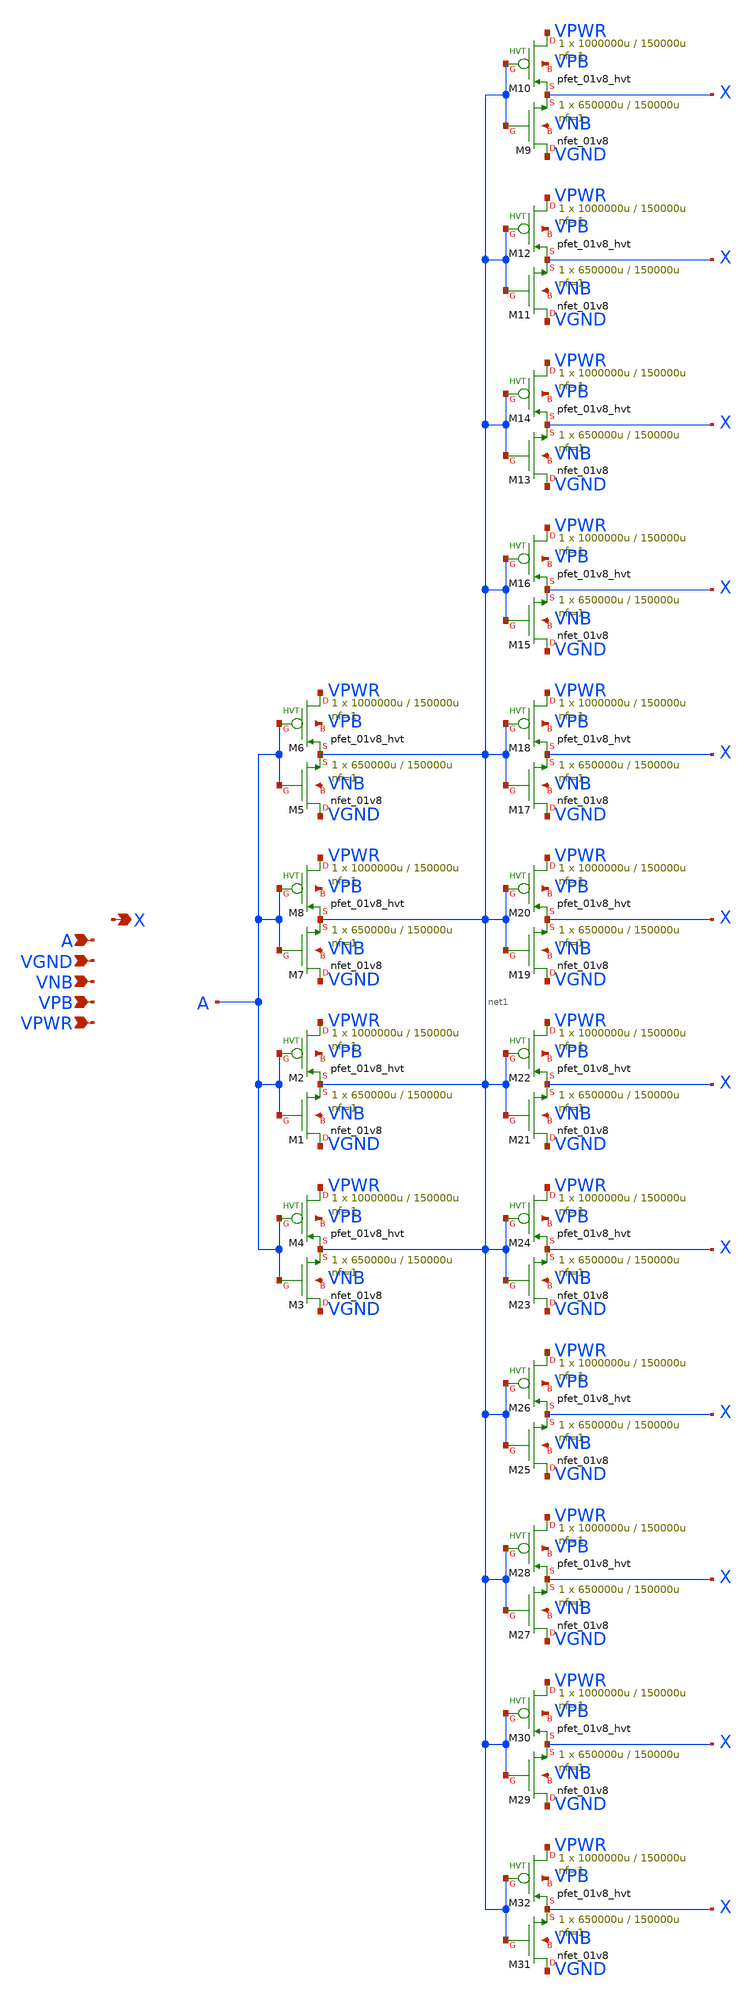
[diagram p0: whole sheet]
** sch_path: schematics/buf/sky130_fd_sc_hd__buf_12.sch
**.subckt sky130_fd_sc_hd__buf_12 A VGND VNB VPB VPWR X
*.ipin A
*.ipin VGND
*.ipin VNB
*.ipin VPB
*.ipin VPWR
*.opin X
XM1 VGND A net1 VNB sky130_fd_pr__nfet_01v8 L=150000u W=650000u nf=1 ad='int((1 + 1)/2) * 650000u / 1 * 0.29'
+ as='int((1 + 2)/2) * 650000u / 1 * 0.29' pd='2*int((1 + 1)/2) * (650000u / 1 + 0.29)' ps='2*int((1 + 2)/2) * (650000u / 1 + 0.29)'
+ nrd='0.29 / 650000u ' nrs='0.29 / 650000u ' sa=0 sb=0 sd=0 mult=1 m=1
XM2 VPWR A net1 VPB sky130_fd_pr__pfet_01v8_hvt L=150000u W=1000000u nf=1 ad='int((1 + 1)/2) * 1000000u / 1 * 0.29'
+ as='int((1 + 2)/2) * 1000000u / 1 * 0.29' pd='2*int((1 + 1)/2) * (1000000u / 1 + 0.29)' ps='2*int((1 + 2)/2) * (1000000u / 1 + 0.29)'
+ nrd='0.29 / 1000000u ' nrs='0.29 / 1000000u ' sa=0 sb=0 sd=0 mult=1 m=1
XM3 VGND A net1 VNB sky130_fd_pr__nfet_01v8 L=150000u W=650000u nf=1 ad='int((1 + 1)/2) * 650000u / 1 * 0.29'
+ as='int((1 + 2)/2) * 650000u / 1 * 0.29' pd='2*int((1 + 1)/2) * (650000u / 1 + 0.29)' ps='2*int((1 + 2)/2) * (650000u / 1 + 0.29)'
+ nrd='0.29 / 650000u ' nrs='0.29 / 650000u ' sa=0 sb=0 sd=0 mult=1 m=1
XM4 VPWR A net1 VPB sky130_fd_pr__pfet_01v8_hvt L=150000u W=1000000u nf=1 ad='int((1 + 1)/2) * 1000000u / 1 * 0.29'
+ as='int((1 + 2)/2) * 1000000u / 1 * 0.29' pd='2*int((1 + 1)/2) * (1000000u / 1 + 0.29)' ps='2*int((1 + 2)/2) * (1000000u / 1 + 0.29)'
+ nrd='0.29 / 1000000u ' nrs='0.29 / 1000000u ' sa=0 sb=0 sd=0 mult=1 m=1
XM5 VGND A net1 VNB sky130_fd_pr__nfet_01v8 L=150000u W=650000u nf=1 ad='int((1 + 1)/2) * 650000u / 1 * 0.29'
+ as='int((1 + 2)/2) * 650000u / 1 * 0.29' pd='2*int((1 + 1)/2) * (650000u / 1 + 0.29)' ps='2*int((1 + 2)/2) * (650000u / 1 + 0.29)'
+ nrd='0.29 / 650000u ' nrs='0.29 / 650000u ' sa=0 sb=0 sd=0 mult=1 m=1
XM6 VPWR A net1 VPB sky130_fd_pr__pfet_01v8_hvt L=150000u W=1000000u nf=1 ad='int((1 + 1)/2) * 1000000u / 1 * 0.29'
+ as='int((1 + 2)/2) * 1000000u / 1 * 0.29' pd='2*int((1 + 1)/2) * (1000000u / 1 + 0.29)' ps='2*int((1 + 2)/2) * (1000000u / 1 + 0.29)'
+ nrd='0.29 / 1000000u ' nrs='0.29 / 1000000u ' sa=0 sb=0 sd=0 mult=1 m=1
XM7 VGND A net1 VNB sky130_fd_pr__nfet_01v8 L=150000u W=650000u nf=1 ad='int((1 + 1)/2) * 650000u / 1 * 0.29'
+ as='int((1 + 2)/2) * 650000u / 1 * 0.29' pd='2*int((1 + 1)/2) * (650000u / 1 + 0.29)' ps='2*int((1 + 2)/2) * (650000u / 1 + 0.29)'
+ nrd='0.29 / 650000u ' nrs='0.29 / 650000u ' sa=0 sb=0 sd=0 mult=1 m=1
XM8 VPWR A net1 VPB sky130_fd_pr__pfet_01v8_hvt L=150000u W=1000000u nf=1 ad='int((1 + 1)/2) * 1000000u / 1 * 0.29'
+ as='int((1 + 2)/2) * 1000000u / 1 * 0.29' pd='2*int((1 + 1)/2) * (1000000u / 1 + 0.29)' ps='2*int((1 + 2)/2) * (1000000u / 1 + 0.29)'
+ nrd='0.29 / 1000000u ' nrs='0.29 / 1000000u ' sa=0 sb=0 sd=0 mult=1 m=1
XM9 VGND net1 X VNB sky130_fd_pr__nfet_01v8 L=150000u W=650000u nf=1 ad='int((1 + 1)/2) * 650000u / 1 * 0.29'
+ as='int((1 + 2)/2) * 650000u / 1 * 0.29' pd='2*int((1 + 1)/2) * (650000u / 1 + 0.29)' ps='2*int((1 + 2)/2) * (650000u / 1 + 0.29)'
+ nrd='0.29 / 650000u ' nrs='0.29 / 650000u ' sa=0 sb=0 sd=0 mult=1 m=1
XM10 VPWR net1 X VPB sky130_fd_pr__pfet_01v8_hvt L=150000u W=1000000u nf=1 ad='int((1 + 1)/2) * 1000000u / 1 * 0.29'
+ as='int((1 + 2)/2) * 1000000u / 1 * 0.29' pd='2*int((1 + 1)/2) * (1000000u / 1 + 0.29)' ps='2*int((1 + 2)/2) * (1000000u / 1 + 0.29)'
+ nrd='0.29 / 1000000u ' nrs='0.29 / 1000000u ' sa=0 sb=0 sd=0 mult=1 m=1
XM11 VGND net1 X VNB sky130_fd_pr__nfet_01v8 L=150000u W=650000u nf=1 ad='int((1 + 1)/2) * 650000u / 1 * 0.29'
+ as='int((1 + 2)/2) * 650000u / 1 * 0.29' pd='2*int((1 + 1)/2) * (650000u / 1 + 0.29)' ps='2*int((1 + 2)/2) * (650000u / 1 + 0.29)'
+ nrd='0.29 / 650000u ' nrs='0.29 / 650000u ' sa=0 sb=0 sd=0 mult=1 m=1
XM12 VPWR net1 X VPB sky130_fd_pr__pfet_01v8_hvt L=150000u W=1000000u nf=1 ad='int((1 + 1)/2) * 1000000u / 1 * 0.29'
+ as='int((1 + 2)/2) * 1000000u / 1 * 0.29' pd='2*int((1 + 1)/2) * (1000000u / 1 + 0.29)' ps='2*int((1 + 2)/2) * (1000000u / 1 + 0.29)'
+ nrd='0.29 / 1000000u ' nrs='0.29 / 1000000u ' sa=0 sb=0 sd=0 mult=1 m=1
XM13 VGND net1 X VNB sky130_fd_pr__nfet_01v8 L=150000u W=650000u nf=1 ad='int((1 + 1)/2) * 650000u / 1 * 0.29'
+ as='int((1 + 2)/2) * 650000u / 1 * 0.29' pd='2*int((1 + 1)/2) * (650000u / 1 + 0.29)' ps='2*int((1 + 2)/2) * (650000u / 1 + 0.29)'
+ nrd='0.29 / 650000u ' nrs='0.29 / 650000u ' sa=0 sb=0 sd=0 mult=1 m=1
XM14 VPWR net1 X VPB sky130_fd_pr__pfet_01v8_hvt L=150000u W=1000000u nf=1 ad='int((1 + 1)/2) * 1000000u / 1 * 0.29'
+ as='int((1 + 2)/2) * 1000000u / 1 * 0.29' pd='2*int((1 + 1)/2) * (1000000u / 1 + 0.29)' ps='2*int((1 + 2)/2) * (1000000u / 1 + 0.29)'
+ nrd='0.29 / 1000000u ' nrs='0.29 / 1000000u ' sa=0 sb=0 sd=0 mult=1 m=1
XM15 VGND net1 X VNB sky130_fd_pr__nfet_01v8 L=150000u W=650000u nf=1 ad='int((1 + 1)/2) * 650000u / 1 * 0.29'
+ as='int((1 + 2)/2) * 650000u / 1 * 0.29' pd='2*int((1 + 1)/2) * (650000u / 1 + 0.29)' ps='2*int((1 + 2)/2) * (650000u / 1 + 0.29)'
+ nrd='0.29 / 650000u ' nrs='0.29 / 650000u ' sa=0 sb=0 sd=0 mult=1 m=1
XM16 VPWR net1 X VPB sky130_fd_pr__pfet_01v8_hvt L=150000u W=1000000u nf=1 ad='int((1 + 1)/2) * 1000000u / 1 * 0.29'
+ as='int((1 + 2)/2) * 1000000u / 1 * 0.29' pd='2*int((1 + 1)/2) * (1000000u / 1 + 0.29)' ps='2*int((1 + 2)/2) * (1000000u / 1 + 0.29)'
+ nrd='0.29 / 1000000u ' nrs='0.29 / 1000000u ' sa=0 sb=0 sd=0 mult=1 m=1
XM17 VGND net1 X VNB sky130_fd_pr__nfet_01v8 L=150000u W=650000u nf=1 ad='int((1 + 1)/2) * 650000u / 1 * 0.29'
+ as='int((1 + 2)/2) * 650000u / 1 * 0.29' pd='2*int((1 + 1)/2) * (650000u / 1 + 0.29)' ps='2*int((1 + 2)/2) * (650000u / 1 + 0.29)'
+ nrd='0.29 / 650000u ' nrs='0.29 / 650000u ' sa=0 sb=0 sd=0 mult=1 m=1
XM18 VPWR net1 X VPB sky130_fd_pr__pfet_01v8_hvt L=150000u W=1000000u nf=1 ad='int((1 + 1)/2) * 1000000u / 1 * 0.29'
+ as='int((1 + 2)/2) * 1000000u / 1 * 0.29' pd='2*int((1 + 1)/2) * (1000000u / 1 + 0.29)' ps='2*int((1 + 2)/2) * (1000000u / 1 + 0.29)'
+ nrd='0.29 / 1000000u ' nrs='0.29 / 1000000u ' sa=0 sb=0 sd=0 mult=1 m=1
XM19 VGND net1 X VNB sky130_fd_pr__nfet_01v8 L=150000u W=650000u nf=1 ad='int((1 + 1)/2) * 650000u / 1 * 0.29'
+ as='int((1 + 2)/2) * 650000u / 1 * 0.29' pd='2*int((1 + 1)/2) * (650000u / 1 + 0.29)' ps='2*int((1 + 2)/2) * (650000u / 1 + 0.29)'
+ nrd='0.29 / 650000u ' nrs='0.29 / 650000u ' sa=0 sb=0 sd=0 mult=1 m=1
XM20 VPWR net1 X VPB sky130_fd_pr__pfet_01v8_hvt L=150000u W=1000000u nf=1 ad='int((1 + 1)/2) * 1000000u / 1 * 0.29'
+ as='int((1 + 2)/2) * 1000000u / 1 * 0.29' pd='2*int((1 + 1)/2) * (1000000u / 1 + 0.29)' ps='2*int((1 + 2)/2) * (1000000u / 1 + 0.29)'
+ nrd='0.29 / 1000000u ' nrs='0.29 / 1000000u ' sa=0 sb=0 sd=0 mult=1 m=1
XM21 VGND net1 X VNB sky130_fd_pr__nfet_01v8 L=150000u W=650000u nf=1 ad='int((1 + 1)/2) * 650000u / 1 * 0.29'
+ as='int((1 + 2)/2) * 650000u / 1 * 0.29' pd='2*int((1 + 1)/2) * (650000u / 1 + 0.29)' ps='2*int((1 + 2)/2) * (650000u / 1 + 0.29)'
+ nrd='0.29 / 650000u ' nrs='0.29 / 650000u ' sa=0 sb=0 sd=0 mult=1 m=1
XM22 VPWR net1 X VPB sky130_fd_pr__pfet_01v8_hvt L=150000u W=1000000u nf=1 ad='int((1 + 1)/2) * 1000000u / 1 * 0.29'
+ as='int((1 + 2)/2) * 1000000u / 1 * 0.29' pd='2*int((1 + 1)/2) * (1000000u / 1 + 0.29)' ps='2*int((1 + 2)/2) * (1000000u / 1 + 0.29)'
+ nrd='0.29 / 1000000u ' nrs='0.29 / 1000000u ' sa=0 sb=0 sd=0 mult=1 m=1
XM23 VGND net1 X VNB sky130_fd_pr__nfet_01v8 L=150000u W=650000u nf=1 ad='int((1 + 1)/2) * 650000u / 1 * 0.29'
+ as='int((1 + 2)/2) * 650000u / 1 * 0.29' pd='2*int((1 + 1)/2) * (650000u / 1 + 0.29)' ps='2*int((1 + 2)/2) * (650000u / 1 + 0.29)'
+ nrd='0.29 / 650000u ' nrs='0.29 / 650000u ' sa=0 sb=0 sd=0 mult=1 m=1
XM24 VPWR net1 X VPB sky130_fd_pr__pfet_01v8_hvt L=150000u W=1000000u nf=1 ad='int((1 + 1)/2) * 1000000u / 1 * 0.29'
+ as='int((1 + 2)/2) * 1000000u / 1 * 0.29' pd='2*int((1 + 1)/2) * (1000000u / 1 + 0.29)' ps='2*int((1 + 2)/2) * (1000000u / 1 + 0.29)'
+ nrd='0.29 / 1000000u ' nrs='0.29 / 1000000u ' sa=0 sb=0 sd=0 mult=1 m=1
XM25 VGND net1 X VNB sky130_fd_pr__nfet_01v8 L=150000u W=650000u nf=1 ad='int((1 + 1)/2) * 650000u / 1 * 0.29'
+ as='int((1 + 2)/2) * 650000u / 1 * 0.29' pd='2*int((1 + 1)/2) * (650000u / 1 + 0.29)' ps='2*int((1 + 2)/2) * (650000u / 1 + 0.29)'
+ nrd='0.29 / 650000u ' nrs='0.29 / 650000u ' sa=0 sb=0 sd=0 mult=1 m=1
XM26 VPWR net1 X VPB sky130_fd_pr__pfet_01v8_hvt L=150000u W=1000000u nf=1 ad='int((1 + 1)/2) * 1000000u / 1 * 0.29'
+ as='int((1 + 2)/2) * 1000000u / 1 * 0.29' pd='2*int((1 + 1)/2) * (1000000u / 1 + 0.29)' ps='2*int((1 + 2)/2) * (1000000u / 1 + 0.29)'
+ nrd='0.29 / 1000000u ' nrs='0.29 / 1000000u ' sa=0 sb=0 sd=0 mult=1 m=1
XM27 VGND net1 X VNB sky130_fd_pr__nfet_01v8 L=150000u W=650000u nf=1 ad='int((1 + 1)/2) * 650000u / 1 * 0.29'
+ as='int((1 + 2)/2) * 650000u / 1 * 0.29' pd='2*int((1 + 1)/2) * (650000u / 1 + 0.29)' ps='2*int((1 + 2)/2) * (650000u / 1 + 0.29)'
+ nrd='0.29 / 650000u ' nrs='0.29 / 650000u ' sa=0 sb=0 sd=0 mult=1 m=1
XM28 VPWR net1 X VPB sky130_fd_pr__pfet_01v8_hvt L=150000u W=1000000u nf=1 ad='int((1 + 1)/2) * 1000000u / 1 * 0.29'
+ as='int((1 + 2)/2) * 1000000u / 1 * 0.29' pd='2*int((1 + 1)/2) * (1000000u / 1 + 0.29)' ps='2*int((1 + 2)/2) * (1000000u / 1 + 0.29)'
+ nrd='0.29 / 1000000u ' nrs='0.29 / 1000000u ' sa=0 sb=0 sd=0 mult=1 m=1
XM29 VGND net1 X VNB sky130_fd_pr__nfet_01v8 L=150000u W=650000u nf=1 ad='int((1 + 1)/2) * 650000u / 1 * 0.29'
+ as='int((1 + 2)/2) * 650000u / 1 * 0.29' pd='2*int((1 + 1)/2) * (650000u / 1 + 0.29)' ps='2*int((1 + 2)/2) * (650000u / 1 + 0.29)'
+ nrd='0.29 / 650000u ' nrs='0.29 / 650000u ' sa=0 sb=0 sd=0 mult=1 m=1
XM30 VPWR net1 X VPB sky130_fd_pr__pfet_01v8_hvt L=150000u W=1000000u nf=1 ad='int((1 + 1)/2) * 1000000u / 1 * 0.29'
+ as='int((1 + 2)/2) * 1000000u / 1 * 0.29' pd='2*int((1 + 1)/2) * (1000000u / 1 + 0.29)' ps='2*int((1 + 2)/2) * (1000000u / 1 + 0.29)'
+ nrd='0.29 / 1000000u ' nrs='0.29 / 1000000u ' sa=0 sb=0 sd=0 mult=1 m=1
XM31 VGND net1 X VNB sky130_fd_pr__nfet_01v8 L=150000u W=650000u nf=1 ad='int((1 + 1)/2) * 650000u / 1 * 0.29'
+ as='int((1 + 2)/2) * 650000u / 1 * 0.29' pd='2*int((1 + 1)/2) * (650000u / 1 + 0.29)' ps='2*int((1 + 2)/2) * (650000u / 1 + 0.29)'
+ nrd='0.29 / 650000u ' nrs='0.29 / 650000u ' sa=0 sb=0 sd=0 mult=1 m=1
XM32 VPWR net1 X VPB sky130_fd_pr__pfet_01v8_hvt L=150000u W=1000000u nf=1 ad='int((1 + 1)/2) * 1000000u / 1 * 0.29'
+ as='int((1 + 2)/2) * 1000000u / 1 * 0.29' pd='2*int((1 + 1)/2) * (1000000u / 1 + 0.29)' ps='2*int((1 + 2)/2) * (1000000u / 1 + 0.29)'
+ nrd='0.29 / 1000000u ' nrs='0.29 / 1000000u ' sa=0 sb=0 sd=0 mult=1 m=1
**.ends
.end
